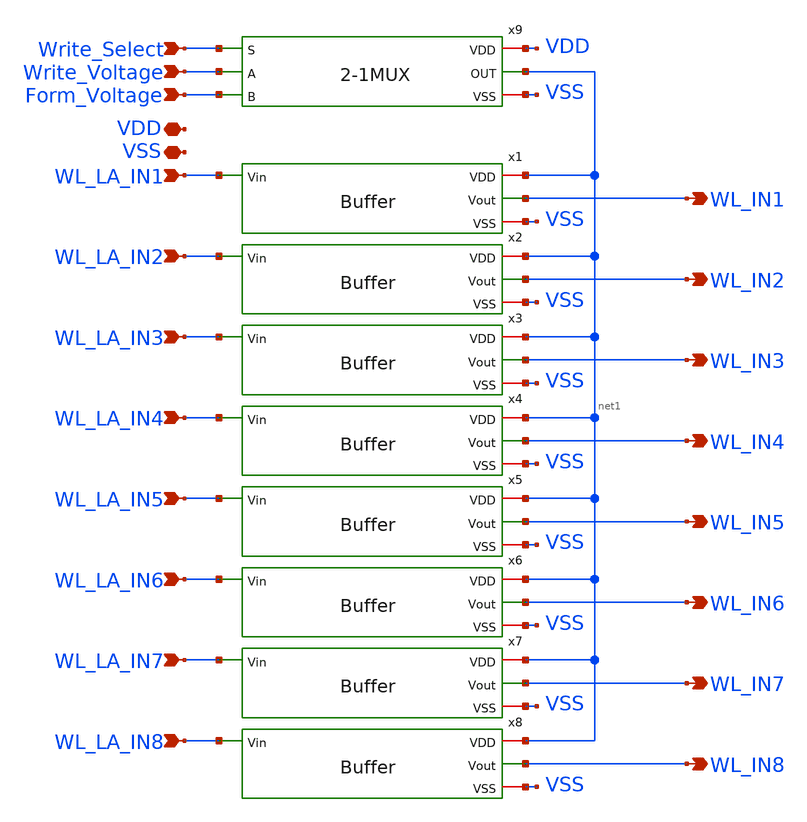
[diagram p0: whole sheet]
** sch_path: xschem/8LineWordInput.sch
**.subckt 8LineWordInput WL_LA_IN1 WL_LA_IN2 WL_LA_IN3 WL_LA_IN4 WL_LA_IN5 WL_LA_IN6 WL_LA_IN7
*+ WL_LA_IN8 WL_IN1 WL_IN2 WL_IN3 WL_IN4 WL_IN5 WL_IN6 WL_IN7 WL_IN8 VDD VSS Write_Select Write_Voltage
*+ Form_Voltage
*.ipin WL_LA_IN1
*.ipin WL_LA_IN2
*.ipin WL_LA_IN3
*.ipin WL_LA_IN4
*.ipin WL_LA_IN5
*.ipin WL_LA_IN6
*.ipin WL_LA_IN7
*.ipin WL_LA_IN8
*.opin WL_IN1
*.opin WL_IN2
*.opin WL_IN3
*.opin WL_IN4
*.opin WL_IN5
*.opin WL_IN6
*.opin WL_IN7
*.opin WL_IN8
*.iopin VDD
*.iopin VSS
*.ipin Write_Select
*.ipin Write_Voltage
*.ipin Form_Voltage
x1 net1 WL_LA_IN1 WL_IN1 VSS Buffer
x2 net1 WL_LA_IN2 WL_IN2 VSS Buffer
x3 net1 WL_LA_IN3 WL_IN3 VSS Buffer
x4 net1 WL_LA_IN4 WL_IN4 VSS Buffer
x5 net1 WL_LA_IN5 WL_IN5 VSS Buffer
x6 net1 WL_LA_IN6 WL_IN6 VSS Buffer
x7 net1 WL_LA_IN7 WL_IN7 VSS Buffer
x8 net1 WL_LA_IN8 WL_IN8 VSS Buffer
x9 VDD Write_Select Write_Voltage net1 Form_Voltage VSS 2-1MUX
**.ends

* expanding   symbol:  Buffer.sym # of pins=4
** sym_path: xschem/Buffer.sym
** sch_path: xschem/Buffer.sch
.subckt Buffer VDD Vin Vout VSS
*.iopin VDD
*.iopin VSS
*.ipin Vin
*.opin Vout
x1 VDD Vin net1 VSS Inverter
x2 VDD net1 Vout VSS Inverter
.ends


* expanding   symbol:  2-1MUX.sym # of pins=6
** sym_path: xschem/2-1MUX.sym
** sch_path: xschem/2-1MUX.sch
.subckt 2-1MUX VDD S A OUT B VSS
*.ipin A
*.ipin B
*.ipin S
*.iopin VDD
*.iopin VSS
*.opin OUT
x1 net1 VDD OUT A VSS S TransmissionGate
x2 S VDD OUT B VSS net1 TransmissionGate
x3 VDD S net1 VSS Inverter
.ends


* expanding   symbol:  Inverter.sym # of pins=4
** sym_path: xschem/Inverter.sym
** sch_path: xschem/Inverter.sch
.subckt Inverter VDD Vin Vout VSS
*.ipin Vin
*.iopin VDD
*.iopin VSS
*.opin Vout
XM1 Vout Vin VSS VSS sky130_fd_pr__nfet_g5v0d10v5 L=0.5 W=0.75 nf=1 ad='int((nf+1)/2) * W/nf * 0.29'
+ as='int((nf+2)/2) * W/nf * 0.29' pd='2*int((nf+1)/2) * (W/nf + 0.29)' ps='2*int((nf+2)/2) * (W/nf + 0.29)'
+ nrd='0.29 / W' nrs='0.29 / W' sa=0 sb=0 sd=0 mult=1 m=1
XM2 Vout Vin VDD VDD sky130_fd_pr__pfet_g5v0d10v5 L=0.5 W=1.5 nf=1 ad='int((nf+1)/2) * W/nf * 0.29' as='int((nf+2)/2) * W/nf * 0.29'
+ pd='2*int((nf+1)/2) * (W/nf + 0.29)' ps='2*int((nf+2)/2) * (W/nf + 0.29)' nrd='0.29 / W' nrs='0.29 / W'
+ sa=0 sb=0 sd=0 mult=1 m=1
.ends


* expanding   symbol:  TransmissionGate.sym # of pins=6
** sym_path: xschem/TransmissionGate.sym
** sch_path: xschem/TransmissionGate.sch
.subckt TransmissionGate SP VDD Out In VSS SN
*.opin Out
*.ipin In
*.ipin SP
*.iopin VDD
*.iopin VSS
*.ipin SN
XM1 In SN Out VSS sky130_fd_pr__nfet_g5v0d10v5 L=0.5 W=0.75 nf=1 ad='int((nf+1)/2) * W/nf * 0.29' as='int((nf+2)/2) * W/nf * 0.29'
+ pd='2*int((nf+1)/2) * (W/nf + 0.29)' ps='2*int((nf+2)/2) * (W/nf + 0.29)' nrd='0.29 / W' nrs='0.29 / W'
+ sa=0 sb=0 sd=0 mult=1 m=1
XM2 In SP Out VDD sky130_fd_pr__pfet_g5v0d10v5 L=0.5 W=1.5 nf=1 ad='int((nf+1)/2) * W/nf * 0.29' as='int((nf+2)/2) * W/nf * 0.29'
+ pd='2*int((nf+1)/2) * (W/nf + 0.29)' ps='2*int((nf+2)/2) * (W/nf + 0.29)' nrd='0.29 / W' nrs='0.29 / W'
+ sa=0 sb=0 sd=0 mult=1 m=1
.ends

.end
